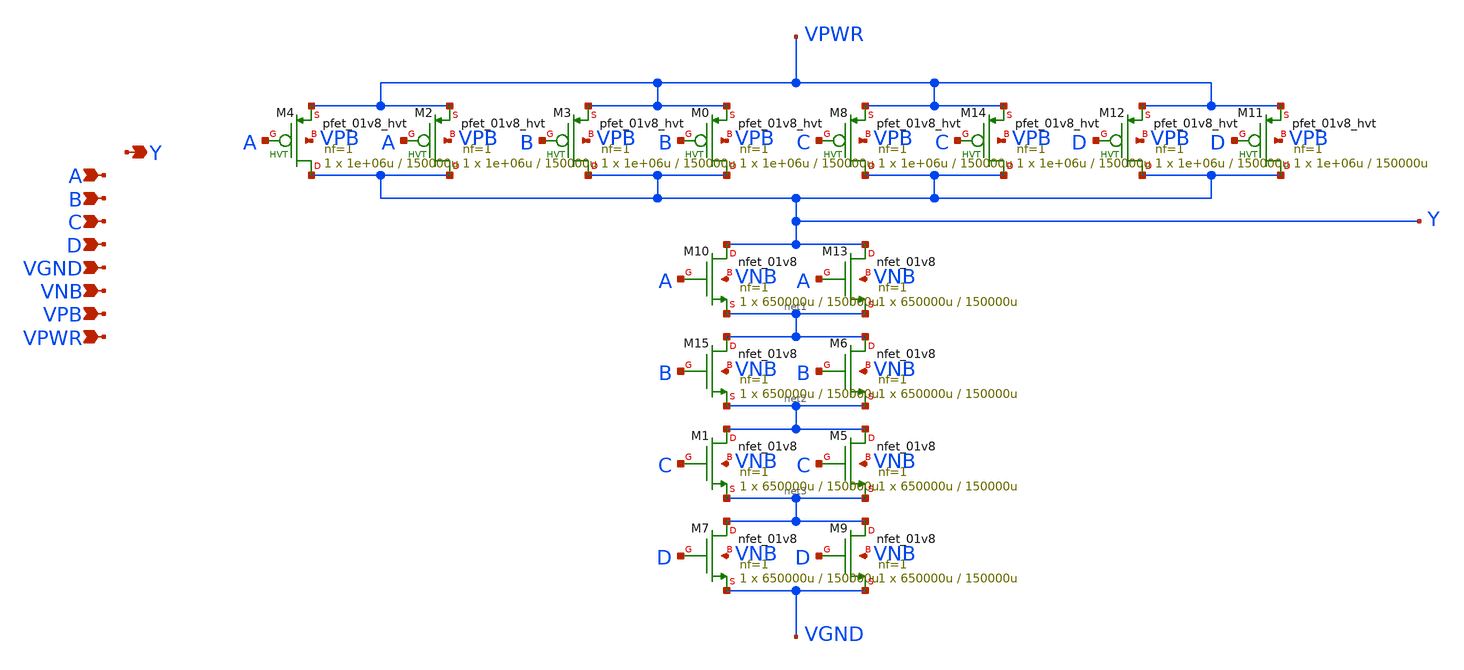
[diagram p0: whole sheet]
** sch_path: schematics/nand4/sky130_fd_sc_hd__nand4_2.sch
**.subckt sky130_fd_sc_hd__nand4_2 A B C D VGND VNB VPB VPWR Y
*.ipin A
*.ipin B
*.ipin C
*.ipin D
*.ipin VGND
*.ipin VNB
*.ipin VPB
*.ipin VPWR
*.opin Y
XM0 Y B VPWR VPB sky130_fd_pr__pfet_01v8_hvt L=150000u W=1e+06u nf=1 ad='int((1 + 1)/2) * 1e+06u / 1 * 0.29'
+ as='int((1 + 2)/2) * 1e+06u / 1 * 0.29' pd='2*int((1 + 1)/2) * (1e+06u / 1 + 0.29)' ps='2*int((1 + 2)/2) * (1e+06u / 1 + 0.29)'
+ nrd='0.29 / 1e+06u ' nrs='0.29 / 1e+06u ' sa=0 sb=0 sd=0 mult=1 m=1
XM1 net2 C net3 VNB sky130_fd_pr__nfet_01v8 L=150000u W=650000u nf=1 ad='int((1 + 1)/2) * 650000u / 1 * 0.29'
+ as='int((1 + 2)/2) * 650000u / 1 * 0.29' pd='2*int((1 + 1)/2) * (650000u / 1 + 0.29)' ps='2*int((1 + 2)/2) * (650000u / 1 + 0.29)'
+ nrd='0.29 / 650000u ' nrs='0.29 / 650000u ' sa=0 sb=0 sd=0 mult=1 m=1
XM2 Y A VPWR VPB sky130_fd_pr__pfet_01v8_hvt L=150000u W=1e+06u nf=1 ad='int((1 + 1)/2) * 1e+06u / 1 * 0.29'
+ as='int((1 + 2)/2) * 1e+06u / 1 * 0.29' pd='2*int((1 + 1)/2) * (1e+06u / 1 + 0.29)' ps='2*int((1 + 2)/2) * (1e+06u / 1 + 0.29)'
+ nrd='0.29 / 1e+06u ' nrs='0.29 / 1e+06u ' sa=0 sb=0 sd=0 mult=1 m=1
XM3 Y B VPWR VPB sky130_fd_pr__pfet_01v8_hvt L=150000u W=1e+06u nf=1 ad='int((1 + 1)/2) * 1e+06u / 1 * 0.29'
+ as='int((1 + 2)/2) * 1e+06u / 1 * 0.29' pd='2*int((1 + 1)/2) * (1e+06u / 1 + 0.29)' ps='2*int((1 + 2)/2) * (1e+06u / 1 + 0.29)'
+ nrd='0.29 / 1e+06u ' nrs='0.29 / 1e+06u ' sa=0 sb=0 sd=0 mult=1 m=1
XM4 Y A VPWR VPB sky130_fd_pr__pfet_01v8_hvt L=150000u W=1e+06u nf=1 ad='int((1 + 1)/2) * 1e+06u / 1 * 0.29'
+ as='int((1 + 2)/2) * 1e+06u / 1 * 0.29' pd='2*int((1 + 1)/2) * (1e+06u / 1 + 0.29)' ps='2*int((1 + 2)/2) * (1e+06u / 1 + 0.29)'
+ nrd='0.29 / 1e+06u ' nrs='0.29 / 1e+06u ' sa=0 sb=0 sd=0 mult=1 m=1
XM5 net2 C net3 VNB sky130_fd_pr__nfet_01v8 L=150000u W=650000u nf=1 ad='int((1 + 1)/2) * 650000u / 1 * 0.29'
+ as='int((1 + 2)/2) * 650000u / 1 * 0.29' pd='2*int((1 + 1)/2) * (650000u / 1 + 0.29)' ps='2*int((1 + 2)/2) * (650000u / 1 + 0.29)'
+ nrd='0.29 / 650000u ' nrs='0.29 / 650000u ' sa=0 sb=0 sd=0 mult=1 m=1
XM6 net1 B net2 VNB sky130_fd_pr__nfet_01v8 L=150000u W=650000u nf=1 ad='int((1 + 1)/2) * 650000u / 1 * 0.29'
+ as='int((1 + 2)/2) * 650000u / 1 * 0.29' pd='2*int((1 + 1)/2) * (650000u / 1 + 0.29)' ps='2*int((1 + 2)/2) * (650000u / 1 + 0.29)'
+ nrd='0.29 / 650000u ' nrs='0.29 / 650000u ' sa=0 sb=0 sd=0 mult=1 m=1
XM7 net3 D VGND VNB sky130_fd_pr__nfet_01v8 L=150000u W=650000u nf=1 ad='int((1 + 1)/2) * 650000u / 1 * 0.29'
+ as='int((1 + 2)/2) * 650000u / 1 * 0.29' pd='2*int((1 + 1)/2) * (650000u / 1 + 0.29)' ps='2*int((1 + 2)/2) * (650000u / 1 + 0.29)'
+ nrd='0.29 / 650000u ' nrs='0.29 / 650000u ' sa=0 sb=0 sd=0 mult=1 m=1
XM8 Y C VPWR VPB sky130_fd_pr__pfet_01v8_hvt L=150000u W=1e+06u nf=1 ad='int((1 + 1)/2) * 1e+06u / 1 * 0.29'
+ as='int((1 + 2)/2) * 1e+06u / 1 * 0.29' pd='2*int((1 + 1)/2) * (1e+06u / 1 + 0.29)' ps='2*int((1 + 2)/2) * (1e+06u / 1 + 0.29)'
+ nrd='0.29 / 1e+06u ' nrs='0.29 / 1e+06u ' sa=0 sb=0 sd=0 mult=1 m=1
XM9 net3 D VGND VNB sky130_fd_pr__nfet_01v8 L=150000u W=650000u nf=1 ad='int((1 + 1)/2) * 650000u / 1 * 0.29'
+ as='int((1 + 2)/2) * 650000u / 1 * 0.29' pd='2*int((1 + 1)/2) * (650000u / 1 + 0.29)' ps='2*int((1 + 2)/2) * (650000u / 1 + 0.29)'
+ nrd='0.29 / 650000u ' nrs='0.29 / 650000u ' sa=0 sb=0 sd=0 mult=1 m=1
XM10 Y A net1 VNB sky130_fd_pr__nfet_01v8 L=150000u W=650000u nf=1 ad='int((1 + 1)/2) * 650000u / 1 * 0.29'
+ as='int((1 + 2)/2) * 650000u / 1 * 0.29' pd='2*int((1 + 1)/2) * (650000u / 1 + 0.29)' ps='2*int((1 + 2)/2) * (650000u / 1 + 0.29)'
+ nrd='0.29 / 650000u ' nrs='0.29 / 650000u ' sa=0 sb=0 sd=0 mult=1 m=1
XM11 Y D VPWR VPB sky130_fd_pr__pfet_01v8_hvt L=150000u W=1e+06u nf=1 ad='int((1 + 1)/2) * 1e+06u / 1 * 0.29'
+ as='int((1 + 2)/2) * 1e+06u / 1 * 0.29' pd='2*int((1 + 1)/2) * (1e+06u / 1 + 0.29)' ps='2*int((1 + 2)/2) * (1e+06u / 1 + 0.29)'
+ nrd='0.29 / 1e+06u ' nrs='0.29 / 1e+06u ' sa=0 sb=0 sd=0 mult=1 m=1
XM12 Y D VPWR VPB sky130_fd_pr__pfet_01v8_hvt L=150000u W=1e+06u nf=1 ad='int((1 + 1)/2) * 1e+06u / 1 * 0.29'
+ as='int((1 + 2)/2) * 1e+06u / 1 * 0.29' pd='2*int((1 + 1)/2) * (1e+06u / 1 + 0.29)' ps='2*int((1 + 2)/2) * (1e+06u / 1 + 0.29)'
+ nrd='0.29 / 1e+06u ' nrs='0.29 / 1e+06u ' sa=0 sb=0 sd=0 mult=1 m=1
XM13 Y A net1 VNB sky130_fd_pr__nfet_01v8 L=150000u W=650000u nf=1 ad='int((1 + 1)/2) * 650000u / 1 * 0.29'
+ as='int((1 + 2)/2) * 650000u / 1 * 0.29' pd='2*int((1 + 1)/2) * (650000u / 1 + 0.29)' ps='2*int((1 + 2)/2) * (650000u / 1 + 0.29)'
+ nrd='0.29 / 650000u ' nrs='0.29 / 650000u ' sa=0 sb=0 sd=0 mult=1 m=1
XM14 Y C VPWR VPB sky130_fd_pr__pfet_01v8_hvt L=150000u W=1e+06u nf=1 ad='int((1 + 1)/2) * 1e+06u / 1 * 0.29'
+ as='int((1 + 2)/2) * 1e+06u / 1 * 0.29' pd='2*int((1 + 1)/2) * (1e+06u / 1 + 0.29)' ps='2*int((1 + 2)/2) * (1e+06u / 1 + 0.29)'
+ nrd='0.29 / 1e+06u ' nrs='0.29 / 1e+06u ' sa=0 sb=0 sd=0 mult=1 m=1
XM15 net1 B net2 VNB sky130_fd_pr__nfet_01v8 L=150000u W=650000u nf=1 ad='int((1 + 1)/2) * 650000u / 1 * 0.29'
+ as='int((1 + 2)/2) * 650000u / 1 * 0.29' pd='2*int((1 + 1)/2) * (650000u / 1 + 0.29)' ps='2*int((1 + 2)/2) * (650000u / 1 + 0.29)'
+ nrd='0.29 / 650000u ' nrs='0.29 / 650000u ' sa=0 sb=0 sd=0 mult=1 m=1
**.ends
.end
